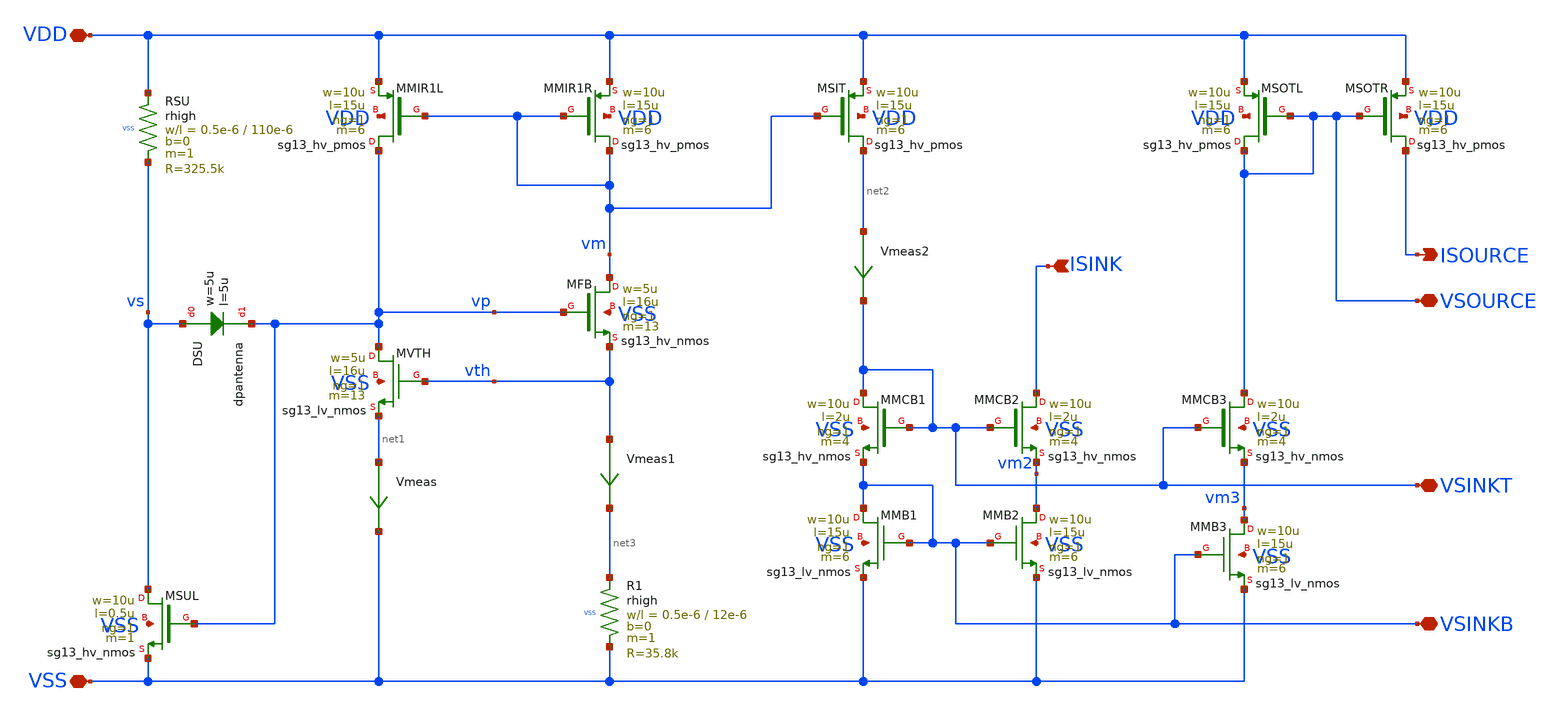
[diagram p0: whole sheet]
** sch_path: ip/vthref/xschem/vthref.sch
**.subckt vthref VSS VDD ISINK ISOURCE VSOURCE VSINKT VSINKB
*.iopin VSS
*.iopin VDD
*.ipin ISINK
*.opin ISOURCE
*.iopin VSOURCE
*.iopin VSINKT
*.iopin VSINKB
XMMIR1L vp vm VDD VDD sg13_hv_pmos w=10u l=15u ng=1 m=6 mm_ok=1
XMMIR1R vm vm VDD VDD sg13_hv_pmos w=10u l=15u ng=1 m=6 mm_ok=1
XMSIT net2 vm VDD VDD sg13_hv_pmos w=10u l=15u ng=1 m=6 mm_ok=1
XMSOTL VSOURCE VSOURCE VDD VDD sg13_hv_pmos w=10u l=15u ng=1 m=6 mm_ok=1
XMSOTR ISOURCE VSOURCE VDD VDD sg13_hv_pmos w=10u l=15u ng=1 m=6 mm_ok=1
XMFB vm vp vth VSS sg13_hv_nmos w=5u l=16u ng=1 m=13 mm_ok=1
XMVTH vp vth net1 VSS sg13_lv_nmos w=5u l=16u ng=1 m=13 mm_ok=1
XMMB1 VSINKB VSINKB VSS VSS sg13_lv_nmos w=10u l=15u ng=1 m=6 mm_ok=1
XMMB2 vm2 VSINKB VSS VSS sg13_lv_nmos w=10u l=15u ng=1 m=6 mm_ok=1
XMMB3 vm3 VSINKB VSS VSS sg13_lv_nmos w=10u l=15u ng=1 m=6 mm_ok=1
XMMCB1 VSINKT VSINKT VSINKB VSS sg13_hv_nmos w=10u l=2u ng=1 m=4 mm_ok=1
XMMCB2 ISINK VSINKT vm2 VSS sg13_hv_nmos w=10u l=2u ng=1 m=4 mm_ok=1
XMMCB3 VSOURCE VSINKT vm3 VSS sg13_hv_nmos w=10u l=2u ng=1 m=4 mm_ok=1
XMSUL vs vp VSS VSS sg13_hv_nmos w=10u l=0.5u ng=1 m=1 mm_ok=1
Vmeas net1 VSS 0
.save i(vmeas)
Vmeas1 vth net3 0
.save i(vmeas1)
Vmeas2 net2 VSINKT 0
.save i(vmeas2)
XDSU vs vp dpantenna l=5u w=5u
XRSU VDD vs VSS rhigh w=0.5e-6 l=110e-6 m=1 b=0 mm_ok=1
XR1 net3 VSS VSS rhigh w=0.5e-6 l=12e-6 m=1 b=0 mm_ok=1
**.ends
.end
